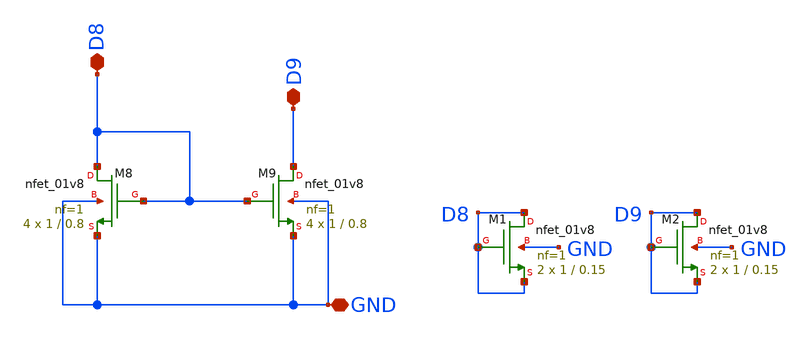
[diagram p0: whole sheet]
** sch_path: opamp/xschem/nmoscs2.sch
**.subckt nmoscs2 GND D9 D8
*.iopin GND
*.iopin D9
*.iopin D8
XM9 D9 D8 GND GND sky130_fd_pr__nfet_01v8 L=0.8 W=1 nf=1 ad='int((nf+1)/2) * W/nf * 0.29' as='int((nf+2)/2) * W/nf * 0.29'
+ pd='2*int((nf+1)/2) * (W/nf + 0.29)' ps='2*int((nf+2)/2) * (W/nf + 0.29)' nrd='0.29 / W' nrs='0.29 / W'
+ sa=0 sb=0 sd=0 mult=4 m=4
XM8 D8 D8 GND GND sky130_fd_pr__nfet_01v8 L=0.8 W=1 nf=1 ad='int((nf+1)/2) * W/nf * 0.29' as='int((nf+2)/2) * W/nf * 0.29'
+ pd='2*int((nf+1)/2) * (W/nf + 0.29)' ps='2*int((nf+2)/2) * (W/nf + 0.29)' nrd='0.29 / W' nrs='0.29 / W'
+ sa=0 sb=0 sd=0 mult=4 m=4
XM1 D8 D8 D8 GND sky130_fd_pr__nfet_01v8 L=0.15 W=1 nf=1 ad='int((nf+1)/2) * W/nf * 0.29' as='int((nf+2)/2) * W/nf * 0.29'
+ pd='2*int((nf+1)/2) * (W/nf + 0.29)' ps='2*int((nf+2)/2) * (W/nf + 0.29)' nrd='0.29 / W' nrs='0.29 / W'
+ sa=0 sb=0 sd=0 mult=2 m=2
XM2 D9 D9 D9 GND sky130_fd_pr__nfet_01v8 L=0.15 W=1 nf=1 ad='int((nf+1)/2) * W/nf * 0.29' as='int((nf+2)/2) * W/nf * 0.29'
+ pd='2*int((nf+1)/2) * (W/nf + 0.29)' ps='2*int((nf+2)/2) * (W/nf + 0.29)' nrd='0.29 / W' nrs='0.29 / W'
+ sa=0 sb=0 sd=0 mult=2 m=2
**.ends
.end
